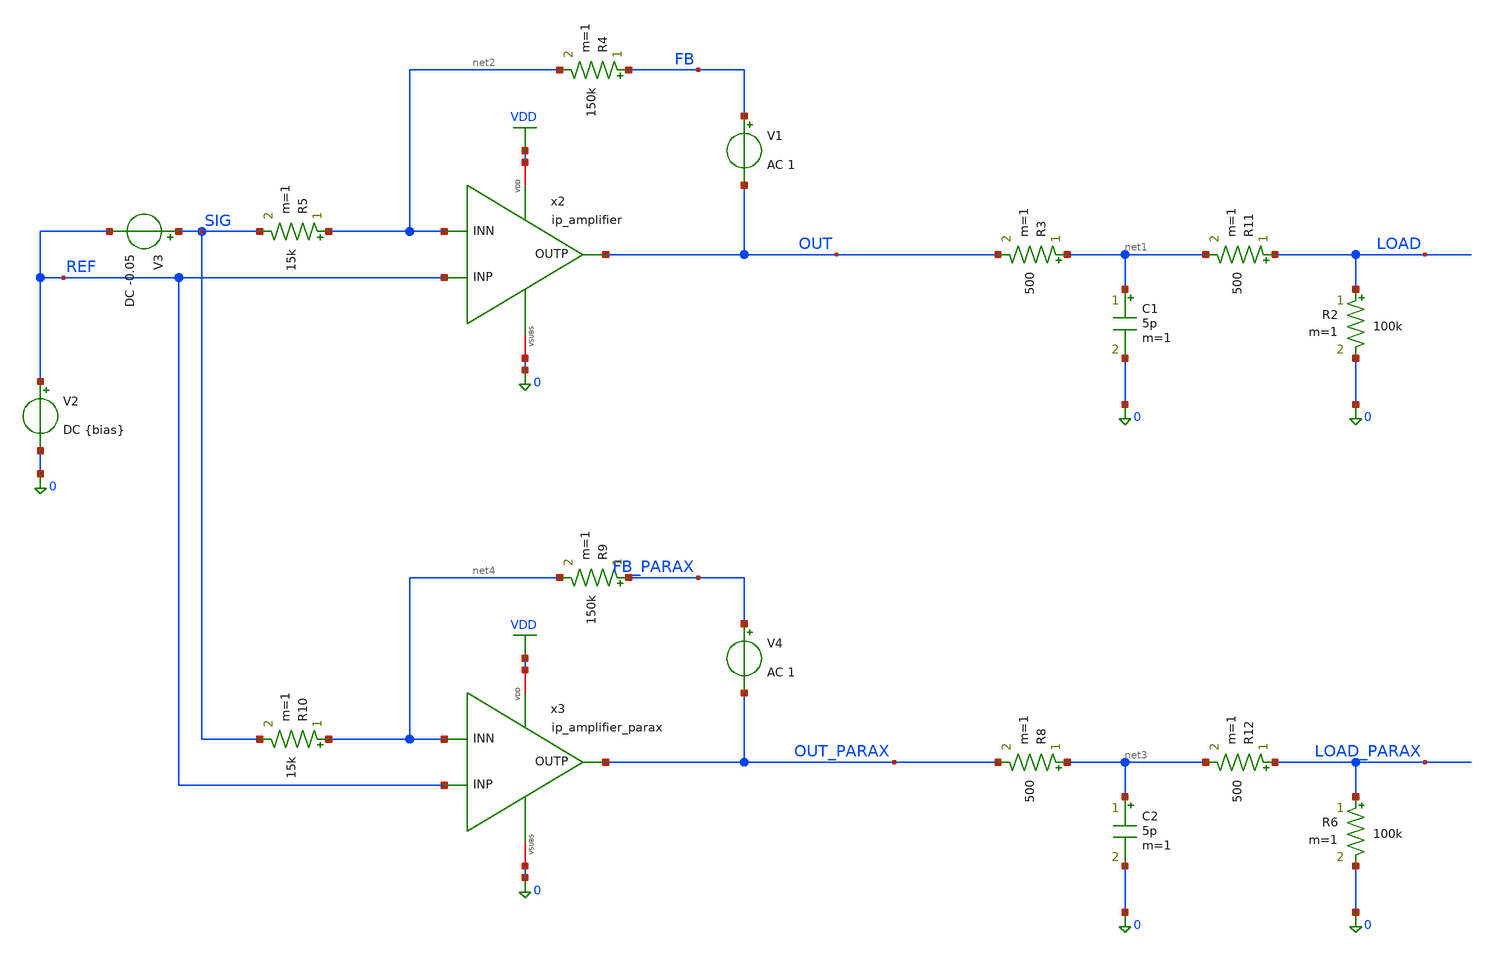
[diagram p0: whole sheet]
** sch_path: xschem/tb_amplifier_x10_ac.sch
**.subckt tb_amplifier_x10_ac
V2 REF 0 DC {bias}
x2 VDD 0 REF net2 OUT ip_amplifier
R2 LOAD 0 100k m=1
V1 FB OUT AC 1
R3 net1 OUT 500 m=1
C1 net1 0 5p m=1
R4 FB net2 150k m=1
R5 net2 SIG 15k m=1
V3 SIG REF DC -0.05
R6 LOAD_PARAX 0 100k m=1
V4 FB_PARAX OUT_PARAX AC 1
R8 net3 OUT_PARAX 500 m=1
C2 net3 0 5p m=1
R9 FB_PARAX net4 150k m=1
R10 net4 SIG 15k m=1
x3 VDD 0 REF net4 OUT_PARAX ip_amplifier_parax
R11 LOAD net1 500 m=1
R12 LOAD_PARAX net3 500 m=1
**** begin user architecture code

.lib $::180MCU_MODELS/sm141064.ngspice statistical
.lib $::180MCU_MODELS/sm141064.ngspice res_statistical
.lib $::180MCU_MODELS/sm141064.ngspice moscap_typical
.lib $::180MCU_MODELS/sm141064.ngspice diode_typical
.lib $::180MCU_MODELS/sm141064.ngspice mimcap_typical




V_DD VDD 0 3.3

# Global parameters typically sourced from design.ngspice
.param sw_stat_global   = 1
.param sw_stat_mismatch = 1
.param mc_skew          = 1
.param res_mc_skew=3
.param cap_mc_skew=3
.param fnoicor=0

.param bias=1.0

.control
	op
	write tb_amplifier_x10_ac.op.raw
  	foreach v_bias 0.5 1.0 1.5
    		alterparam bias=$v_bias
		repeat 10
			mc_source
			ac dec 1000 1000 1e9
			let oltf = v(out) / v(fb)
			let oltf_parax = v(out_parax) / v(fb_parax)
			write tb_amplifier_x10_ac.raw
			set appendwrite
			reset
		end
	end
	quit
.endc



**** end user architecture code
**.ends

* expanding   symbol:  ip_amplifier.sym # of pins=5
** sym_path: ip_amplifier.sym
** sch_path: ip_amplifier.sch
.subckt ip_amplifier VDD VSUBS INP INN OUTP
*.iopin VDD
*.iopin VSUBS
*.ipin INP
*.ipin INN
*.opin OUTP
XM1 COMP INP COMMON_ VDD pfet_03v3 L=5u W=18.0u nf=1 ad='int((nf+1)/2) * W/nf * 0.18u' as='int((nf+2)/2) * W/nf * 0.18u'
+ pd='2*int((nf+1)/2) * (W/nf + 0.18u)' ps='2*int((nf+2)/2) * (W/nf + 0.18u)' nrd='0.18u / W' nrs='0.18u / W'
+ sa=0 sb=0 sd=0 m=1 par=1
XM2 net6 INN COMMON_ VDD pfet_03v3 L=5u W=18.0u nf=1 ad='int((nf+1)/2) * W/nf * 0.18u' as='int((nf+2)/2) * W/nf * 0.18u'
+ pd='2*int((nf+1)/2) * (W/nf + 0.18u)' ps='2*int((nf+2)/2) * (W/nf + 0.18u)' nrd='0.18u / W' nrs='0.18u / W'
+ sa=0 sb=0 sd=0 m=1 par=1
XM3 net2 NBIAS VSUBS vsubs nfet_03v3 L=2u W=6u nf=1 ad='int((nf+1)/2) * W/nf * 0.18u' as='int((nf+2)/2) * W/nf * 0.18u'
+ pd='2*int((nf+1)/2) * (W/nf + 0.18u)' ps='2*int((nf+2)/2) * (W/nf + 0.18u)' nrd='0.18u / W' nrs='0.18u / W'
+ sa=0 sb=0 sd=0 m=2 par=2
XM4 net1 NBIAS VSUBS vsubs nfet_03v3 L=2u W=6u nf=1 ad='int((nf+1)/2) * W/nf * 0.18u' as='int((nf+2)/2) * W/nf * 0.18u'
+ pd='2*int((nf+1)/2) * (W/nf + 0.18u)' ps='2*int((nf+2)/2) * (W/nf + 0.18u)' nrd='0.18u / W' nrs='0.18u / W'
+ sa=0 sb=0 sd=0 m=1 par=1
XM7 NBIAS NBIAS net2 vsubs nfet_03v3 L=0.5u W=6u nf=1 ad='int((nf+1)/2) * W/nf * 0.18u' as='int((nf+2)/2) * W/nf * 0.18u'
+ pd='2*int((nf+1)/2) * (W/nf + 0.18u)' ps='2*int((nf+2)/2) * (W/nf + 0.18u)' nrd='0.18u / W' nrs='0.18u / W'
+ sa=0 sb=0 sd=0 m=4 par=4
XM8 net3 NBIAS net1 vsubs nfet_03v3 L=0.5u W=6u nf=1 ad='int((nf+1)/2) * W/nf * 0.18u' as='int((nf+2)/2) * W/nf * 0.18u'
+ pd='2*int((nf+1)/2) * (W/nf + 0.18u)' ps='2*int((nf+2)/2) * (W/nf + 0.18u)' nrd='0.18u / W' nrs='0.18u / W'
+ sa=0 sb=0 sd=0 m=4 par=4
XM9 net4 PBIAS VDD VDD pfet_03v3 L=2u W=6u nf=1 ad='int((nf+1)/2) * W/nf * 0.18u' as='int((nf+2)/2) * W/nf * 0.18u'
+ pd='2*int((nf+1)/2) * (W/nf + 0.18u)' ps='2*int((nf+2)/2) * (W/nf + 0.18u)' nrd='0.18u / W' nrs='0.18u / W'
+ sa=0 sb=0 sd=0 m=1 par=1
XM10 net5 PBIAS VDD VDD pfet_03v3 L=2u W=6u nf=1 ad='int((nf+1)/2) * W/nf * 0.18u' as='int((nf+2)/2) * W/nf * 0.18u'
+ pd='2*int((nf+1)/2) * (W/nf + 0.18u)' ps='2*int((nf+2)/2) * (W/nf + 0.18u)' nrd='0.18u / W' nrs='0.18u / W'
+ sa=0 sb=0 sd=0 m=1 par=1
XM11 PBIAS PBIAS net4 VDD pfet_03v3 L=0.5u W=6u nf=1 ad='int((nf+1)/2) * W/nf * 0.18u' as='int((nf+2)/2) * W/nf * 0.18u'
+ pd='2*int((nf+1)/2) * (W/nf + 0.18u)' ps='2*int((nf+2)/2) * (W/nf + 0.18u)' nrd='0.18u / W' nrs='0.18u / W'
+ sa=0 sb=0 sd=0 m=4 par=4
XM12 COMMON PBIAS net5 VDD pfet_03v3 L=0.5u W=6u nf=1 ad='int((nf+1)/2) * W/nf * 0.18u' as='int((nf+2)/2) * W/nf * 0.18u'
+ pd='2*int((nf+1)/2) * (W/nf + 0.18u)' ps='2*int((nf+2)/2) * (W/nf + 0.18u)' nrd='0.18u / W' nrs='0.18u / W'
+ sa=0 sb=0 sd=0 m=4 par=4
XM13 COMP net6 VSUBS vsubs nfet_03v3 L=5u W=6u nf=1 ad='int((nf+1)/2) * W/nf * 0.18u' as='int((nf+2)/2) * W/nf * 0.18u'
+ pd='2*int((nf+1)/2) * (W/nf + 0.18u)' ps='2*int((nf+2)/2) * (W/nf + 0.18u)' nrd='0.18u / W' nrs='0.18u / W'
+ sa=0 sb=0 sd=0 m=1 par=1
XM14 net6 net6 VSUBS vsubs nfet_03v3 L=5u W=6u nf=1 ad='int((nf+1)/2) * W/nf * 0.18u' as='int((nf+2)/2) * W/nf * 0.18u'
+ pd='2*int((nf+1)/2) * (W/nf + 0.18u)' ps='2*int((nf+2)/2) * (W/nf + 0.18u)' nrd='0.18u / W' nrs='0.18u / W'
+ sa=0 sb=0 sd=0 m=1 par=1
XM17 net8 PBIAS VDD VDD pfet_03v3 L=0.5u W=12u nf=1 ad='int((nf+1)/2) * W/nf * 0.18u' as='int((nf+2)/2) * W/nf * 0.18u'
+ pd='2*int((nf+1)/2) * (W/nf + 0.18u)' ps='2*int((nf+2)/2) * (W/nf + 0.18u)' nrd='0.18u / W' nrs='0.18u / W'
+ sa=0 sb=0 sd=0 m=2 par=2
XM18 OUTP COMP VSUBS vsubs nfet_03v3 L=0.5u W=12u nf=1 ad='int((nf+1)/2) * W/nf * 0.18u' as='int((nf+2)/2) * W/nf * 0.18u'
+ pd='2*int((nf+1)/2) * (W/nf + 0.18u)' ps='2*int((nf+2)/2) * (W/nf + 0.18u)' nrd='0.18u / W' nrs='0.18u / W'
+ sa=0 sb=0 sd=0 m=4 par=4
XR3 NBIAS net7 vsubs ppolyf_u_1k r_width=1e-6 r_length=48e-6 m=1
Vmeas VDD net7 0
Vmeas1 PBIAS net3 0
Vmeas2 COMMON COMMON_ 0
Vmeas3 net8 OUTP 0
XC1 OUTP COMP cap_mim_2f0_m2m3_noshield c_width=10e-6 c_length=10e-6 m=2
.ends


* expanding   symbol:  ip_amplifier_parax.sym # of pins=5
** sym_path: ip_amplifier.sym
.include [file normalize ./parax/ip_amplifier.sim.spice]
.GLOBAL VDD
.end
